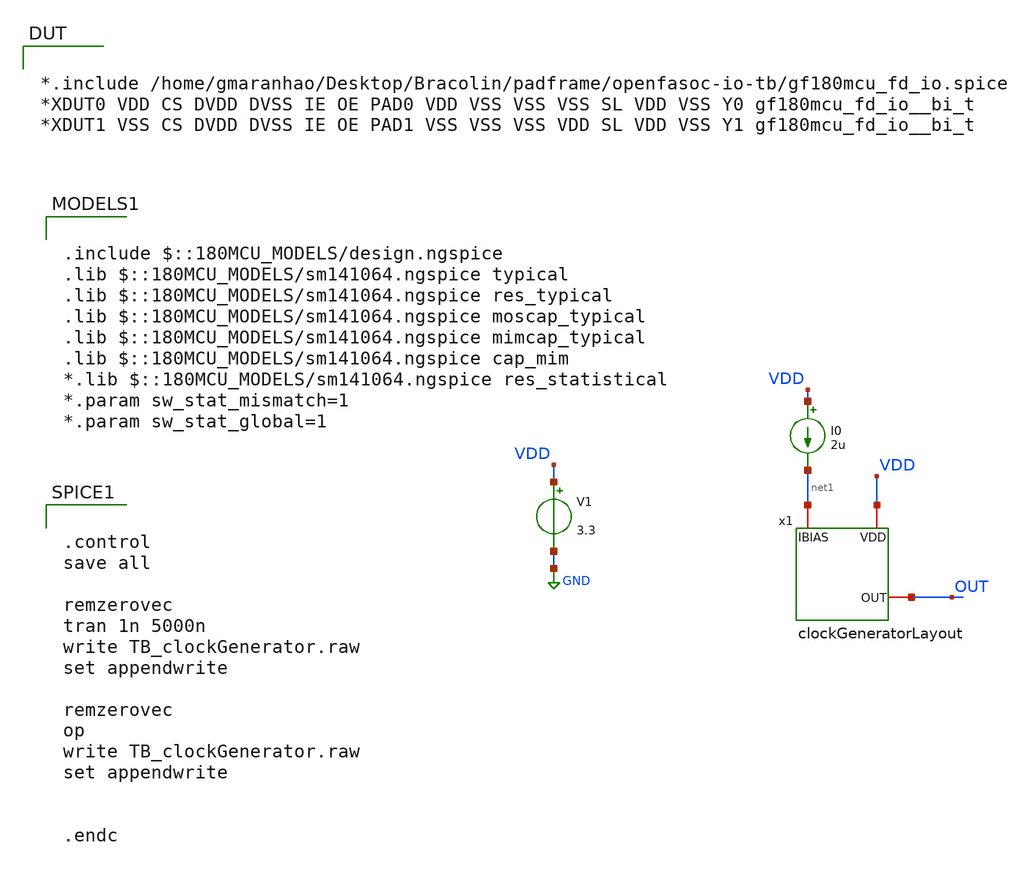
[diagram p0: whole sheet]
** sch_path: Clock_Reference/TB_clockGenerator.sch
**.subckt TB_clockGenerator
x1 VDD OUT net1 clockGeneratorLayout
I0 VDD net1 2u
V1 VDD GND 3.3
**** begin user architecture code


.control
save all

remzerovec
tran 1n 5000n
write TB_clockGenerator.raw
set appendwrite

remzerovec
op
write TB_clockGenerator.raw
set appendwrite


.endc




.include $::180MCU_MODELS/design.ngspice
.lib $::180MCU_MODELS/sm141064.ngspice typical
.lib $::180MCU_MODELS/sm141064.ngspice res_typical
.lib $::180MCU_MODELS/sm141064.ngspice moscap_typical
.lib $::180MCU_MODELS/sm141064.ngspice mimcap_typical
.lib $::180MCU_MODELS/sm141064.ngspice cap_mim
*.lib $::180MCU_MODELS/sm141064.ngspice res_statistical
*.param sw_stat_mismatch=1
*.param sw_stat_global=1



*.include /home/gmaranhao/Desktop/Bracolin/padframe/openfasoc-io-tb/gf180mcu_fd_io.spice
*XDUT0 VDD CS DVDD DVSS IE OE PAD0 VDD VSS VSS VSS SL VDD VSS Y0 gf180mcu_fd_io__bi_t
*XDUT1 VSS CS DVDD DVSS IE OE PAD1 VSS VSS VSS VDD SL VDD VSS Y1 gf180mcu_fd_io__bi_t

**** end user architecture code
**.ends
.GLOBAL GND
.end
